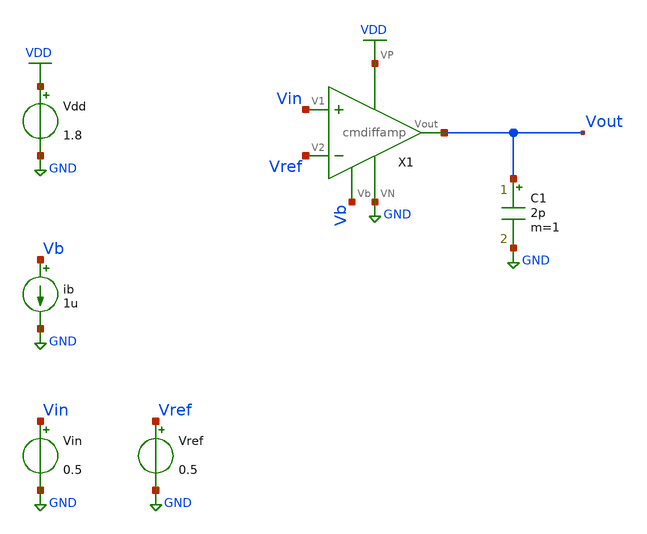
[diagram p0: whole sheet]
** sch_path: projects/current_mirror_diff_amp/xschem_ngspice/cmdiffamp_vtc.sch
**.subckt cmdiffamp_vtc
X1 Vin Vref Vout VDD GND Vb cmdiffamp
Vin Vin GND 0.5
Vref Vref GND 0.5
Vdd VDD GND 1.8
ib Vb GND 1u
C1 Vout GND 2p m=1
**** begin user architecture code



.lib /foss/pdks/sky130A/libs.tech/ngspice/sky130.lib.spice tt

* .dc Vin 0 1.8 0.001 Vref 0.25 0.75 0.25

* .save v(Vout) v(Vref) v(Vin)

.control
compose Vref start=0.25 stop=0.75 step=0.25
foreach val $&Vref
  alter vref $val
  dc vin 0 1.8 0.001
  run
end
.endc

**** end user architecture code
**.ends

* expanding   symbol:
*+  /foss/designs/my_design/projects/current_mirror_diff_amp/xschem_ngspice/cmdiffamp.sym # of pins=6
** sym_path: projects/current_mirror_diff_amp/xschem_ngspice/cmdiffamp.sym
** sch_path: projects/current_mirror_diff_amp/xschem_ngspice/cmdiffamp.sch
.subckt cmdiffamp V1 V2 Vout VP VN Vb
*.ipin V1
*.ipin V2
*.opin Vout
*.iopin VN
*.iopin Vb
*.iopin VP
XM1a net3 V1 net1 VDD sky130_fd_pr__pfet_01v8 L=0.5 W=3 nf=1 ad='int((nf+1)/2) * W/nf * 0.29' as='int((nf+2)/2) * W/nf * 0.29'
+ pd='2*int((nf+1)/2) * (W/nf + 0.29)' ps='2*int((nf+2)/2) * (W/nf + 0.29)' nrd='0.29 / W' nrs='0.29 / W'
+ sa=0 sb=0 sd=0 mult=1 m=1
XM2a net2 V2 net1 VDD sky130_fd_pr__pfet_01v8 L=0.5 W=3 nf=1 ad='int((nf+1)/2) * W/nf * 0.29' as='int((nf+2)/2) * W/nf * 0.29'
+ pd='2*int((nf+1)/2) * (W/nf + 0.29)' ps='2*int((nf+2)/2) * (W/nf + 0.29)' nrd='0.29 / W' nrs='0.29 / W'
+ sa=0 sb=0 sd=0 mult=1 m=1
XM2b net1 V2 net2 VDD sky130_fd_pr__pfet_01v8 L=0.5 W=3 nf=1 ad='int((nf+1)/2) * W/nf * 0.29' as='int((nf+2)/2) * W/nf * 0.29'
+ pd='2*int((nf+1)/2) * (W/nf + 0.29)' ps='2*int((nf+2)/2) * (W/nf + 0.29)' nrd='0.29 / W' nrs='0.29 / W'
+ sa=0 sb=0 sd=0 mult=1 m=1
XM1b net1 V1 net3 VDD sky130_fd_pr__pfet_01v8 L=0.5 W=3 nf=1 ad='int((nf+1)/2) * W/nf * 0.29' as='int((nf+2)/2) * W/nf * 0.29'
+ pd='2*int((nf+1)/2) * (W/nf + 0.29)' ps='2*int((nf+2)/2) * (W/nf + 0.29)' nrd='0.29 / W' nrs='0.29 / W'
+ sa=0 sb=0 sd=0 mult=1 m=1
XM1c net3 V1 net1 VDD sky130_fd_pr__pfet_01v8 L=0.5 W=3 nf=1 ad='int((nf+1)/2) * W/nf * 0.29' as='int((nf+2)/2) * W/nf * 0.29'
+ pd='2*int((nf+1)/2) * (W/nf + 0.29)' ps='2*int((nf+2)/2) * (W/nf + 0.29)' nrd='0.29 / W' nrs='0.29 / W'
+ sa=0 sb=0 sd=0 mult=1 m=1
XM2c net2 V2 net1 VDD sky130_fd_pr__pfet_01v8 L=0.5 W=3 nf=1 ad='int((nf+1)/2) * W/nf * 0.29' as='int((nf+2)/2) * W/nf * 0.29'
+ pd='2*int((nf+1)/2) * (W/nf + 0.29)' ps='2*int((nf+2)/2) * (W/nf + 0.29)' nrd='0.29 / W' nrs='0.29 / W'
+ sa=0 sb=0 sd=0 mult=1 m=1
XM2d net1 V2 net2 VDD sky130_fd_pr__pfet_01v8 L=0.5 W=3 nf=1 ad='int((nf+1)/2) * W/nf * 0.29' as='int((nf+2)/2) * W/nf * 0.29'
+ pd='2*int((nf+1)/2) * (W/nf + 0.29)' ps='2*int((nf+2)/2) * (W/nf + 0.29)' nrd='0.29 / W' nrs='0.29 / W'
+ sa=0 sb=0 sd=0 mult=1 m=1
XM1d net1 V1 net3 VDD sky130_fd_pr__pfet_01v8 L=0.5 W=3 nf=1 ad='int((nf+1)/2) * W/nf * 0.29' as='int((nf+2)/2) * W/nf * 0.29'
+ pd='2*int((nf+1)/2) * (W/nf + 0.29)' ps='2*int((nf+2)/2) * (W/nf + 0.29)' nrd='0.29 / W' nrs='0.29 / W'
+ sa=0 sb=0 sd=0 mult=1 m=1
XM5a net2 net2 VN GND sky130_fd_pr__nfet_01v8 L=0.5 W=3 nf=1 ad='int((nf+1)/2) * W/nf * 0.29' as='int((nf+2)/2) * W/nf * 0.29'
+ pd='2*int((nf+1)/2) * (W/nf + 0.29)' ps='2*int((nf+2)/2) * (W/nf + 0.29)' nrd='0.29 / W' nrs='0.29 / W'
+ sa=0 sb=0 sd=0 mult=1 m=1
XM6a VN net2 net4 GND sky130_fd_pr__nfet_01v8 L=0.5 W=3 nf=1 ad='int((nf+1)/2) * W/nf * 0.29' as='int((nf+2)/2) * W/nf * 0.29'
+ pd='2*int((nf+1)/2) * (W/nf + 0.29)' ps='2*int((nf+2)/2) * (W/nf + 0.29)' nrd='0.29 / W' nrs='0.29 / W'
+ sa=0 sb=0 sd=0 mult=1 m=1
XM6b net4 net2 VN GND sky130_fd_pr__nfet_01v8 L=0.5 W=3 nf=1 ad='int((nf+1)/2) * W/nf * 0.29' as='int((nf+2)/2) * W/nf * 0.29'
+ pd='2*int((nf+1)/2) * (W/nf + 0.29)' ps='2*int((nf+2)/2) * (W/nf + 0.29)' nrd='0.29 / W' nrs='0.29 / W'
+ sa=0 sb=0 sd=0 mult=1 m=1
XM5b VN net2 net2 GND sky130_fd_pr__nfet_01v8 L=0.5 W=3 nf=1 ad='int((nf+1)/2) * W/nf * 0.29' as='int((nf+2)/2) * W/nf * 0.29'
+ pd='2*int((nf+1)/2) * (W/nf + 0.29)' ps='2*int((nf+2)/2) * (W/nf + 0.29)' nrd='0.29 / W' nrs='0.29 / W'
+ sa=0 sb=0 sd=0 mult=1 m=1
XM5c net2 net2 VN GND sky130_fd_pr__nfet_01v8 L=0.5 W=3 nf=1 ad='int((nf+1)/2) * W/nf * 0.29' as='int((nf+2)/2) * W/nf * 0.29'
+ pd='2*int((nf+1)/2) * (W/nf + 0.29)' ps='2*int((nf+2)/2) * (W/nf + 0.29)' nrd='0.29 / W' nrs='0.29 / W'
+ sa=0 sb=0 sd=0 mult=1 m=1
XM6c VN net2 net4 GND sky130_fd_pr__nfet_01v8 L=0.5 W=3 nf=1 ad='int((nf+1)/2) * W/nf * 0.29' as='int((nf+2)/2) * W/nf * 0.29'
+ pd='2*int((nf+1)/2) * (W/nf + 0.29)' ps='2*int((nf+2)/2) * (W/nf + 0.29)' nrd='0.29 / W' nrs='0.29 / W'
+ sa=0 sb=0 sd=0 mult=1 m=1
XM6d net4 net2 VN GND sky130_fd_pr__nfet_01v8 L=0.5 W=3 nf=1 ad='int((nf+1)/2) * W/nf * 0.29' as='int((nf+2)/2) * W/nf * 0.29'
+ pd='2*int((nf+1)/2) * (W/nf + 0.29)' ps='2*int((nf+2)/2) * (W/nf + 0.29)' nrd='0.29 / W' nrs='0.29 / W'
+ sa=0 sb=0 sd=0 mult=1 m=1
XM5d VN net2 net2 GND sky130_fd_pr__nfet_01v8 L=0.5 W=3 nf=1 ad='int((nf+1)/2) * W/nf * 0.29' as='int((nf+2)/2) * W/nf * 0.29'
+ pd='2*int((nf+1)/2) * (W/nf + 0.29)' ps='2*int((nf+2)/2) * (W/nf + 0.29)' nrd='0.29 / W' nrs='0.29 / W'
+ sa=0 sb=0 sd=0 mult=1 m=1
XM3a net3 net3 VN GND sky130_fd_pr__nfet_01v8 L=0.5 W=3 nf=1 ad='int((nf+1)/2) * W/nf * 0.29' as='int((nf+2)/2) * W/nf * 0.29'
+ pd='2*int((nf+1)/2) * (W/nf + 0.29)' ps='2*int((nf+2)/2) * (W/nf + 0.29)' nrd='0.29 / W' nrs='0.29 / W'
+ sa=0 sb=0 sd=0 mult=1 m=1
XM4a VN net3 Vout GND sky130_fd_pr__nfet_01v8 L=0.5 W=3 nf=1 ad='int((nf+1)/2) * W/nf * 0.29' as='int((nf+2)/2) * W/nf * 0.29'
+ pd='2*int((nf+1)/2) * (W/nf + 0.29)' ps='2*int((nf+2)/2) * (W/nf + 0.29)' nrd='0.29 / W' nrs='0.29 / W'
+ sa=0 sb=0 sd=0 mult=1 m=1
XM4b Vout net3 VN GND sky130_fd_pr__nfet_01v8 L=0.5 W=3 nf=1 ad='int((nf+1)/2) * W/nf * 0.29' as='int((nf+2)/2) * W/nf * 0.29'
+ pd='2*int((nf+1)/2) * (W/nf + 0.29)' ps='2*int((nf+2)/2) * (W/nf + 0.29)' nrd='0.29 / W' nrs='0.29 / W'
+ sa=0 sb=0 sd=0 mult=1 m=1
XM3b VN net3 net3 GND sky130_fd_pr__nfet_01v8 L=0.5 W=3 nf=1 ad='int((nf+1)/2) * W/nf * 0.29' as='int((nf+2)/2) * W/nf * 0.29'
+ pd='2*int((nf+1)/2) * (W/nf + 0.29)' ps='2*int((nf+2)/2) * (W/nf + 0.29)' nrd='0.29 / W' nrs='0.29 / W'
+ sa=0 sb=0 sd=0 mult=1 m=1
XM3c net3 net3 VN GND sky130_fd_pr__nfet_01v8 L=0.5 W=3 nf=1 ad='int((nf+1)/2) * W/nf * 0.29' as='int((nf+2)/2) * W/nf * 0.29'
+ pd='2*int((nf+1)/2) * (W/nf + 0.29)' ps='2*int((nf+2)/2) * (W/nf + 0.29)' nrd='0.29 / W' nrs='0.29 / W'
+ sa=0 sb=0 sd=0 mult=1 m=1
XM4c VN net3 Vout GND sky130_fd_pr__nfet_01v8 L=0.5 W=3 nf=1 ad='int((nf+1)/2) * W/nf * 0.29' as='int((nf+2)/2) * W/nf * 0.29'
+ pd='2*int((nf+1)/2) * (W/nf + 0.29)' ps='2*int((nf+2)/2) * (W/nf + 0.29)' nrd='0.29 / W' nrs='0.29 / W'
+ sa=0 sb=0 sd=0 mult=1 m=1
XM4d Vout net3 VN GND sky130_fd_pr__nfet_01v8 L=0.5 W=3 nf=1 ad='int((nf+1)/2) * W/nf * 0.29' as='int((nf+2)/2) * W/nf * 0.29'
+ pd='2*int((nf+1)/2) * (W/nf + 0.29)' ps='2*int((nf+2)/2) * (W/nf + 0.29)' nrd='0.29 / W' nrs='0.29 / W'
+ sa=0 sb=0 sd=0 mult=1 m=1
XM3d VN net3 net3 GND sky130_fd_pr__nfet_01v8 L=0.5 W=3 nf=1 ad='int((nf+1)/2) * W/nf * 0.29' as='int((nf+2)/2) * W/nf * 0.29'
+ pd='2*int((nf+1)/2) * (W/nf + 0.29)' ps='2*int((nf+2)/2) * (W/nf + 0.29)' nrd='0.29 / W' nrs='0.29 / W'
+ sa=0 sb=0 sd=0 mult=1 m=1
XM7a net4 net4 VP VDD sky130_fd_pr__pfet_01v8 L=0.5 W=3 nf=1 ad='int((nf+1)/2) * W/nf * 0.29' as='int((nf+2)/2) * W/nf * 0.29'
+ pd='2*int((nf+1)/2) * (W/nf + 0.29)' ps='2*int((nf+2)/2) * (W/nf + 0.29)' nrd='0.29 / W' nrs='0.29 / W'
+ sa=0 sb=0 sd=0 mult=1 m=1
XM8a VP net4 Vout VDD sky130_fd_pr__pfet_01v8 L=0.5 W=3 nf=1 ad='int((nf+1)/2) * W/nf * 0.29' as='int((nf+2)/2) * W/nf * 0.29'
+ pd='2*int((nf+1)/2) * (W/nf + 0.29)' ps='2*int((nf+2)/2) * (W/nf + 0.29)' nrd='0.29 / W' nrs='0.29 / W'
+ sa=0 sb=0 sd=0 mult=1 m=1
XM8b Vout net4 VP VDD sky130_fd_pr__pfet_01v8 L=0.5 W=3 nf=1 ad='int((nf+1)/2) * W/nf * 0.29' as='int((nf+2)/2) * W/nf * 0.29'
+ pd='2*int((nf+1)/2) * (W/nf + 0.29)' ps='2*int((nf+2)/2) * (W/nf + 0.29)' nrd='0.29 / W' nrs='0.29 / W'
+ sa=0 sb=0 sd=0 mult=1 m=1
XM7b VP net4 net4 VDD sky130_fd_pr__pfet_01v8 L=0.5 W=3 nf=1 ad='int((nf+1)/2) * W/nf * 0.29' as='int((nf+2)/2) * W/nf * 0.29'
+ pd='2*int((nf+1)/2) * (W/nf + 0.29)' ps='2*int((nf+2)/2) * (W/nf + 0.29)' nrd='0.29 / W' nrs='0.29 / W'
+ sa=0 sb=0 sd=0 mult=1 m=1
XM7c net4 net4 VP VDD sky130_fd_pr__pfet_01v8 L=0.5 W=3 nf=1 ad='int((nf+1)/2) * W/nf * 0.29' as='int((nf+2)/2) * W/nf * 0.29'
+ pd='2*int((nf+1)/2) * (W/nf + 0.29)' ps='2*int((nf+2)/2) * (W/nf + 0.29)' nrd='0.29 / W' nrs='0.29 / W'
+ sa=0 sb=0 sd=0 mult=1 m=1
XM8c VP net4 Vout VDD sky130_fd_pr__pfet_01v8 L=0.5 W=3 nf=1 ad='int((nf+1)/2) * W/nf * 0.29' as='int((nf+2)/2) * W/nf * 0.29'
+ pd='2*int((nf+1)/2) * (W/nf + 0.29)' ps='2*int((nf+2)/2) * (W/nf + 0.29)' nrd='0.29 / W' nrs='0.29 / W'
+ sa=0 sb=0 sd=0 mult=1 m=1
XM8d Vout net4 VP VDD sky130_fd_pr__pfet_01v8 L=0.5 W=3 nf=1 ad='int((nf+1)/2) * W/nf * 0.29' as='int((nf+2)/2) * W/nf * 0.29'
+ pd='2*int((nf+1)/2) * (W/nf + 0.29)' ps='2*int((nf+2)/2) * (W/nf + 0.29)' nrd='0.29 / W' nrs='0.29 / W'
+ sa=0 sb=0 sd=0 mult=1 m=1
XM7d VP net4 net4 VDD sky130_fd_pr__pfet_01v8 L=0.5 W=3 nf=1 ad='int((nf+1)/2) * W/nf * 0.29' as='int((nf+2)/2) * W/nf * 0.29'
+ pd='2*int((nf+1)/2) * (W/nf + 0.29)' ps='2*int((nf+2)/2) * (W/nf + 0.29)' nrd='0.29 / W' nrs='0.29 / W'
+ sa=0 sb=0 sd=0 mult=1 m=1
XM9a Vb Vb VP VDD sky130_fd_pr__pfet_01v8 L=0.5 W=1.5 nf=1 ad='int((nf+1)/2) * W/nf * 0.29' as='int((nf+2)/2) * W/nf * 0.29'
+ pd='2*int((nf+1)/2) * (W/nf + 0.29)' ps='2*int((nf+2)/2) * (W/nf + 0.29)' nrd='0.29 / W' nrs='0.29 / W'
+ sa=0 sb=0 sd=0 mult=1 m=1
XM10a VP Vb net1 VDD sky130_fd_pr__pfet_01v8 L=0.5 W=1.5 nf=1 ad='int((nf+1)/2) * W/nf * 0.29' as='int((nf+2)/2) * W/nf * 0.29'
+ pd='2*int((nf+1)/2) * (W/nf + 0.29)' ps='2*int((nf+2)/2) * (W/nf + 0.29)' nrd='0.29 / W' nrs='0.29 / W'
+ sa=0 sb=0 sd=0 mult=1 m=1
XM10b net1 Vb VP VDD sky130_fd_pr__pfet_01v8 L=0.5 W=1.5 nf=1 ad='int((nf+1)/2) * W/nf * 0.29' as='int((nf+2)/2) * W/nf * 0.29'
+ pd='2*int((nf+1)/2) * (W/nf + 0.29)' ps='2*int((nf+2)/2) * (W/nf + 0.29)' nrd='0.29 / W' nrs='0.29 / W'
+ sa=0 sb=0 sd=0 mult=1 m=1
XM9b VP Vb Vb VDD sky130_fd_pr__pfet_01v8 L=0.5 W=1.5 nf=1 ad='int((nf+1)/2) * W/nf * 0.29' as='int((nf+2)/2) * W/nf * 0.29'
+ pd='2*int((nf+1)/2) * (W/nf + 0.29)' ps='2*int((nf+2)/2) * (W/nf + 0.29)' nrd='0.29 / W' nrs='0.29 / W'
+ sa=0 sb=0 sd=0 mult=1 m=1
XM9c Vb Vb VP VDD sky130_fd_pr__pfet_01v8 L=0.5 W=1.5 nf=1 ad='int((nf+1)/2) * W/nf * 0.29' as='int((nf+2)/2) * W/nf * 0.29'
+ pd='2*int((nf+1)/2) * (W/nf + 0.29)' ps='2*int((nf+2)/2) * (W/nf + 0.29)' nrd='0.29 / W' nrs='0.29 / W'
+ sa=0 sb=0 sd=0 mult=1 m=1
XM10c VP Vb net1 VDD sky130_fd_pr__pfet_01v8 L=0.5 W=1.5 nf=1 ad='int((nf+1)/2) * W/nf * 0.29' as='int((nf+2)/2) * W/nf * 0.29'
+ pd='2*int((nf+1)/2) * (W/nf + 0.29)' ps='2*int((nf+2)/2) * (W/nf + 0.29)' nrd='0.29 / W' nrs='0.29 / W'
+ sa=0 sb=0 sd=0 mult=1 m=1
XM10d net1 Vb VP VDD sky130_fd_pr__pfet_01v8 L=0.5 W=1.5 nf=1 ad='int((nf+1)/2) * W/nf * 0.29' as='int((nf+2)/2) * W/nf * 0.29'
+ pd='2*int((nf+1)/2) * (W/nf + 0.29)' ps='2*int((nf+2)/2) * (W/nf + 0.29)' nrd='0.29 / W' nrs='0.29 / W'
+ sa=0 sb=0 sd=0 mult=1 m=1
XM9d VP Vb Vb VDD sky130_fd_pr__pfet_01v8 L=0.5 W=1.5 nf=1 ad='int((nf+1)/2) * W/nf * 0.29' as='int((nf+2)/2) * W/nf * 0.29'
+ pd='2*int((nf+1)/2) * (W/nf + 0.29)' ps='2*int((nf+2)/2) * (W/nf + 0.29)' nrd='0.29 / W' nrs='0.29 / W'
+ sa=0 sb=0 sd=0 mult=1 m=1
XM9e Vb Vb VP VDD sky130_fd_pr__pfet_01v8 L=0.5 W=1.5 nf=1 ad='int((nf+1)/2) * W/nf * 0.29' as='int((nf+2)/2) * W/nf * 0.29'
+ pd='2*int((nf+1)/2) * (W/nf + 0.29)' ps='2*int((nf+2)/2) * (W/nf + 0.29)' nrd='0.29 / W' nrs='0.29 / W'
+ sa=0 sb=0 sd=0 mult=1 m=1
XM10e VP Vb net1 VDD sky130_fd_pr__pfet_01v8 L=0.5 W=1.5 nf=1 ad='int((nf+1)/2) * W/nf * 0.29' as='int((nf+2)/2) * W/nf * 0.29'
+ pd='2*int((nf+1)/2) * (W/nf + 0.29)' ps='2*int((nf+2)/2) * (W/nf + 0.29)' nrd='0.29 / W' nrs='0.29 / W'
+ sa=0 sb=0 sd=0 mult=1 m=1
XM10f net1 Vb VP VDD sky130_fd_pr__pfet_01v8 L=0.5 W=1.5 nf=1 ad='int((nf+1)/2) * W/nf * 0.29' as='int((nf+2)/2) * W/nf * 0.29'
+ pd='2*int((nf+1)/2) * (W/nf + 0.29)' ps='2*int((nf+2)/2) * (W/nf + 0.29)' nrd='0.29 / W' nrs='0.29 / W'
+ sa=0 sb=0 sd=0 mult=1 m=1
XM9f VP Vb Vb VDD sky130_fd_pr__pfet_01v8 L=0.5 W=1.5 nf=1 ad='int((nf+1)/2) * W/nf * 0.29' as='int((nf+2)/2) * W/nf * 0.29'
+ pd='2*int((nf+1)/2) * (W/nf + 0.29)' ps='2*int((nf+2)/2) * (W/nf + 0.29)' nrd='0.29 / W' nrs='0.29 / W'
+ sa=0 sb=0 sd=0 mult=1 m=1
XM9g Vb Vb VP VDD sky130_fd_pr__pfet_01v8 L=0.5 W=1.5 nf=1 ad='int((nf+1)/2) * W/nf * 0.29' as='int((nf+2)/2) * W/nf * 0.29'
+ pd='2*int((nf+1)/2) * (W/nf + 0.29)' ps='2*int((nf+2)/2) * (W/nf + 0.29)' nrd='0.29 / W' nrs='0.29 / W'
+ sa=0 sb=0 sd=0 mult=1 m=1
XM10g VP Vb net1 VDD sky130_fd_pr__pfet_01v8 L=0.5 W=1.5 nf=1 ad='int((nf+1)/2) * W/nf * 0.29' as='int((nf+2)/2) * W/nf * 0.29'
+ pd='2*int((nf+1)/2) * (W/nf + 0.29)' ps='2*int((nf+2)/2) * (W/nf + 0.29)' nrd='0.29 / W' nrs='0.29 / W'
+ sa=0 sb=0 sd=0 mult=1 m=1
XM10h net1 Vb VP VDD sky130_fd_pr__pfet_01v8 L=0.5 W=1.5 nf=1 ad='int((nf+1)/2) * W/nf * 0.29' as='int((nf+2)/2) * W/nf * 0.29'
+ pd='2*int((nf+1)/2) * (W/nf + 0.29)' ps='2*int((nf+2)/2) * (W/nf + 0.29)' nrd='0.29 / W' nrs='0.29 / W'
+ sa=0 sb=0 sd=0 mult=1 m=1
XM9h VP Vb Vb VDD sky130_fd_pr__pfet_01v8 L=0.5 W=1.5 nf=1 ad='int((nf+1)/2) * W/nf * 0.29' as='int((nf+2)/2) * W/nf * 0.29'
+ pd='2*int((nf+1)/2) * (W/nf + 0.29)' ps='2*int((nf+2)/2) * (W/nf + 0.29)' nrd='0.29 / W' nrs='0.29 / W'
+ sa=0 sb=0 sd=0 mult=1 m=1
XM1 VP VP Vb VDD sky130_fd_pr__pfet_01v8 L=0.5 W=1.5 nf=1 ad='int((nf+1)/2) * W/nf * 0.29' as='int((nf+2)/2) * W/nf * 0.29'
+ pd='2*int((nf+1)/2) * (W/nf + 0.29)' ps='2*int((nf+2)/2) * (W/nf + 0.29)' nrd='0.29 / W' nrs='0.29 / W'
+ sa=0 sb=0 sd=0 mult=1 m=1
XM2 Vb VP VP VDD sky130_fd_pr__pfet_01v8 L=0.5 W=1.5 nf=1 ad='int((nf+1)/2) * W/nf * 0.29' as='int((nf+2)/2) * W/nf * 0.29'
+ pd='2*int((nf+1)/2) * (W/nf + 0.29)' ps='2*int((nf+2)/2) * (W/nf + 0.29)' nrd='0.29 / W' nrs='0.29 / W'
+ sa=0 sb=0 sd=0 mult=1 m=1
XM3 VP VP Vb VDD sky130_fd_pr__pfet_01v8 L=0.5 W=1.5 nf=1 ad='int((nf+1)/2) * W/nf * 0.29' as='int((nf+2)/2) * W/nf * 0.29'
+ pd='2*int((nf+1)/2) * (W/nf + 0.29)' ps='2*int((nf+2)/2) * (W/nf + 0.29)' nrd='0.29 / W' nrs='0.29 / W'
+ sa=0 sb=0 sd=0 mult=1 m=1
XM4 Vb VP VP VDD sky130_fd_pr__pfet_01v8 L=0.5 W=1.5 nf=1 ad='int((nf+1)/2) * W/nf * 0.29' as='int((nf+2)/2) * W/nf * 0.29'
+ pd='2*int((nf+1)/2) * (W/nf + 0.29)' ps='2*int((nf+2)/2) * (W/nf + 0.29)' nrd='0.29 / W' nrs='0.29 / W'
+ sa=0 sb=0 sd=0 mult=1 m=1
XM5 net4 VP VP VDD sky130_fd_pr__pfet_01v8 L=0.5 W=3 nf=1 ad='int((nf+1)/2) * W/nf * 0.29' as='int((nf+2)/2) * W/nf * 0.29'
+ pd='2*int((nf+1)/2) * (W/nf + 0.29)' ps='2*int((nf+2)/2) * (W/nf + 0.29)' nrd='0.29 / W' nrs='0.29 / W'
+ sa=0 sb=0 sd=0 mult=1 m=1
XM6 net3 VP VP VDD sky130_fd_pr__pfet_01v8 L=0.5 W=3 nf=1 ad='int((nf+1)/2) * W/nf * 0.29' as='int((nf+2)/2) * W/nf * 0.29'
+ pd='2*int((nf+1)/2) * (W/nf + 0.29)' ps='2*int((nf+2)/2) * (W/nf + 0.29)' nrd='0.29 / W' nrs='0.29 / W'
+ sa=0 sb=0 sd=0 mult=1 m=1
XM7 VP VP net4 VDD sky130_fd_pr__pfet_01v8 L=0.5 W=3 nf=1 ad='int((nf+1)/2) * W/nf * 0.29' as='int((nf+2)/2) * W/nf * 0.29'
+ pd='2*int((nf+1)/2) * (W/nf + 0.29)' ps='2*int((nf+2)/2) * (W/nf + 0.29)' nrd='0.29 / W' nrs='0.29 / W'
+ sa=0 sb=0 sd=0 mult=1 m=1
XM8 net2 VN VN GND sky130_fd_pr__nfet_01v8 L=0.5 W=3 nf=1 ad='int((nf+1)/2) * W/nf * 0.29' as='int((nf+2)/2) * W/nf * 0.29'
+ pd='2*int((nf+1)/2) * (W/nf + 0.29)' ps='2*int((nf+2)/2) * (W/nf + 0.29)' nrd='0.29 / W' nrs='0.29 / W'
+ sa=0 sb=0 sd=0 mult=1 m=1
XM9 VN VN net3 GND sky130_fd_pr__nfet_01v8 L=0.5 W=3 nf=1 ad='int((nf+1)/2) * W/nf * 0.29' as='int((nf+2)/2) * W/nf * 0.29'
+ pd='2*int((nf+1)/2) * (W/nf + 0.29)' ps='2*int((nf+2)/2) * (W/nf + 0.29)' nrd='0.29 / W' nrs='0.29 / W'
+ sa=0 sb=0 sd=0 mult=1 m=1
XM10 net3 VP VP VDD sky130_fd_pr__pfet_01v8 L=0.5 W=3 nf=1 ad='int((nf+1)/2) * W/nf * 0.29' as='int((nf+2)/2) * W/nf * 0.29'
+ pd='2*int((nf+1)/2) * (W/nf + 0.29)' ps='2*int((nf+2)/2) * (W/nf + 0.29)' nrd='0.29 / W' nrs='0.29 / W'
+ sa=0 sb=0 sd=0 mult=1 m=1
XM11 VN VN net2 GND sky130_fd_pr__nfet_01v8 L=0.5 W=3 nf=1 ad='int((nf+1)/2) * W/nf * 0.29' as='int((nf+2)/2) * W/nf * 0.29'
+ pd='2*int((nf+1)/2) * (W/nf + 0.29)' ps='2*int((nf+2)/2) * (W/nf + 0.29)' nrd='0.29 / W' nrs='0.29 / W'
+ sa=0 sb=0 sd=0 mult=1 m=1
XM12 net3 VN VN GND sky130_fd_pr__nfet_01v8 L=0.5 W=3 nf=1 ad='int((nf+1)/2) * W/nf * 0.29' as='int((nf+2)/2) * W/nf * 0.29'
+ pd='2*int((nf+1)/2) * (W/nf + 0.29)' ps='2*int((nf+2)/2) * (W/nf + 0.29)' nrd='0.29 / W' nrs='0.29 / W'
+ sa=0 sb=0 sd=0 mult=1 m=1
.ends

.GLOBAL VDD
.GLOBAL GND
.end
